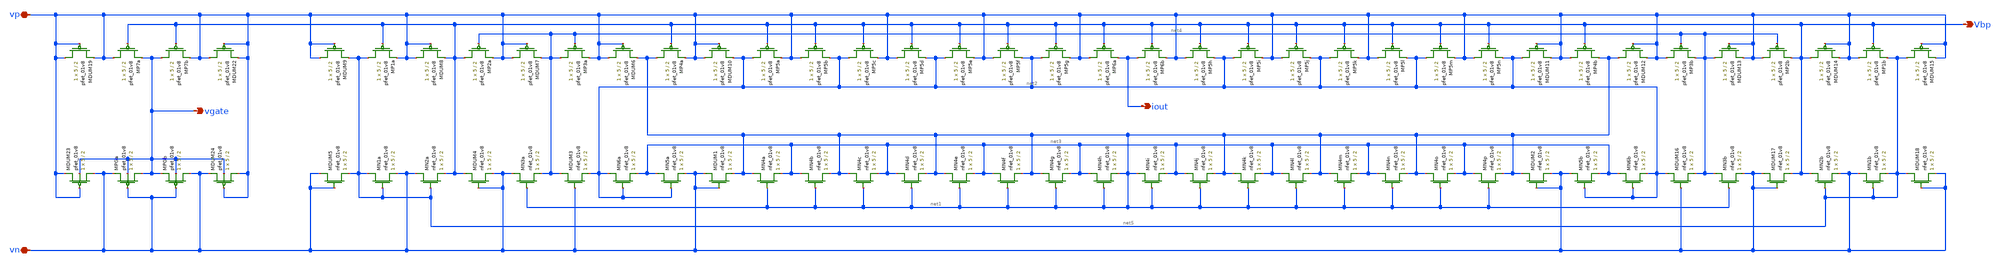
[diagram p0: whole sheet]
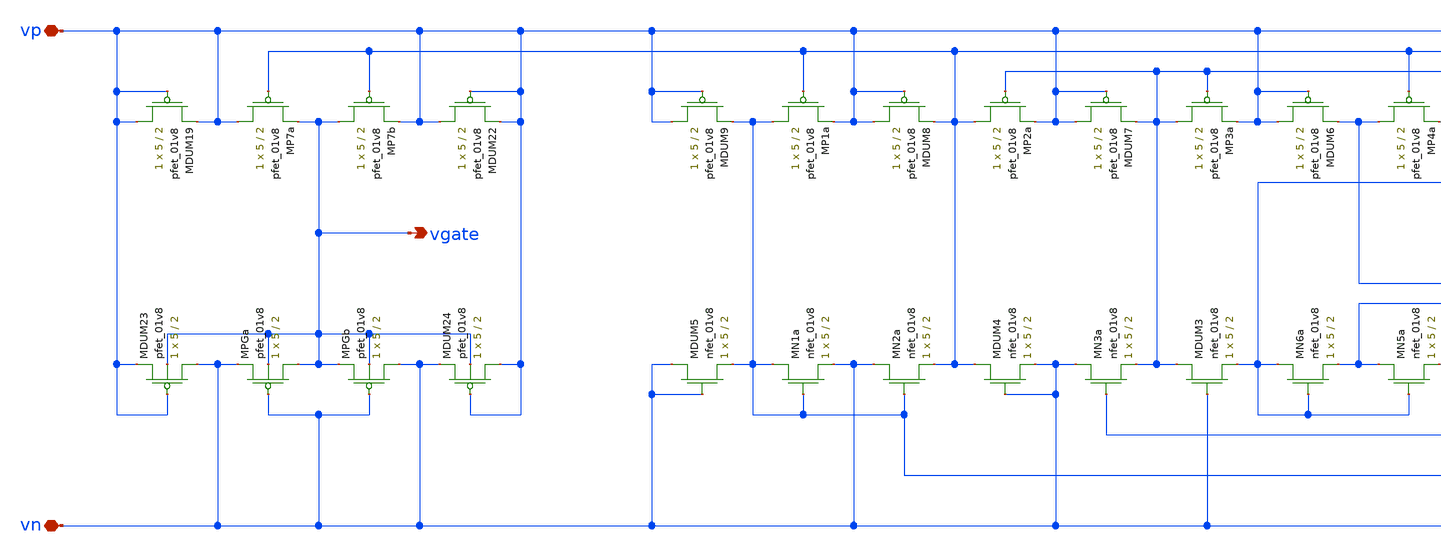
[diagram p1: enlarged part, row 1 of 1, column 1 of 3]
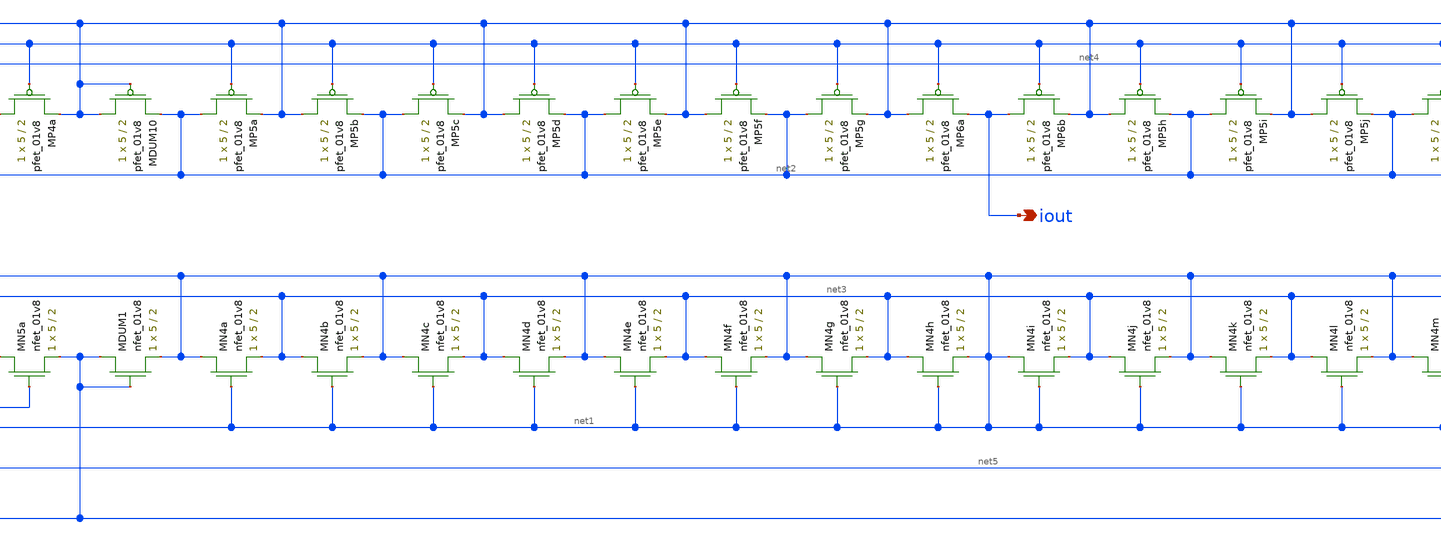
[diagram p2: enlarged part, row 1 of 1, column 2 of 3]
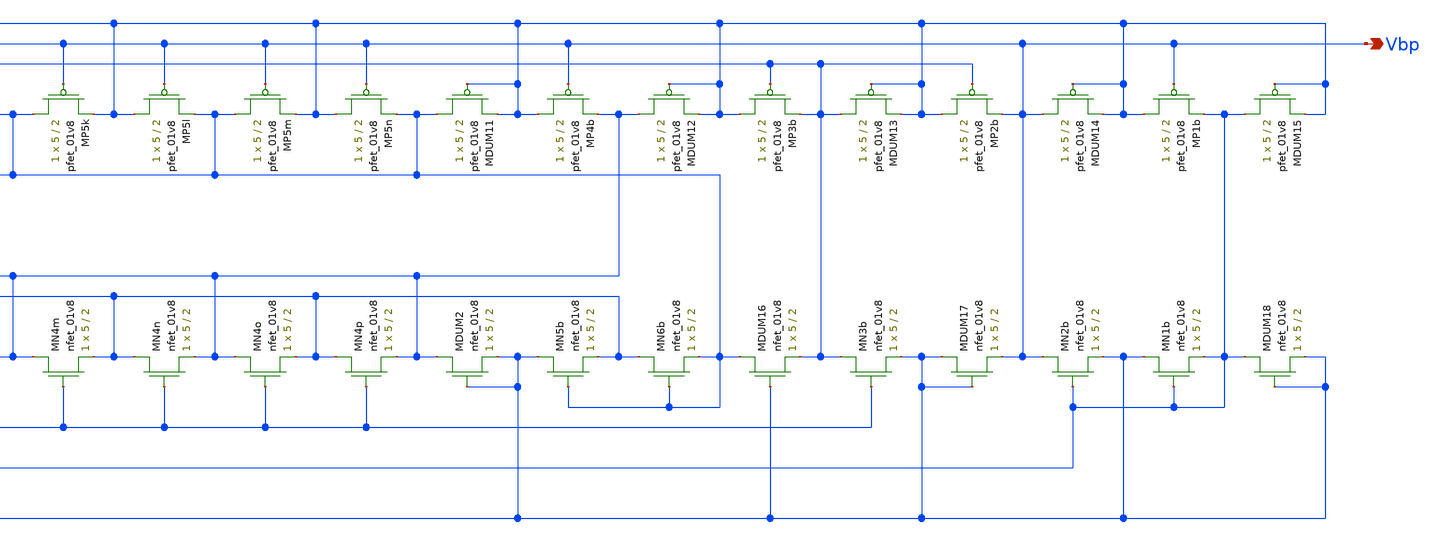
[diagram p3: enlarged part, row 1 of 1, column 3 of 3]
** sch_path: schematic/bias_current_LDS.sch
**.subckt bias_current_LDS iout Vbp vgate vp vn
*.opin iout
*.opin Vbp
*.opin vgate
*.iopin vp
*.iopin vn
XMP1a net5 Vbp vp VDD sky130_fd_pr__pfet_01v8 L=2 W=5 nf=1 ad='int((nf+1)/2) * W/nf * 0.29' as='int((nf+2)/2) * W/nf * 0.29'
+ pd='2*int((nf+1)/2) * (W/nf + 0.29)' ps='2*int((nf+2)/2) * (W/nf + 0.29)' nrd='0.29 / W' nrs='0.29 / W'
+ sa=0 sb=0 sd=0 mult=1 m=1
XMP1b vp Vbp net5 VDD sky130_fd_pr__pfet_01v8 L=2 W=5 nf=1 ad='int((nf+1)/2) * W/nf * 0.29' as='int((nf+2)/2) * W/nf * 0.29'
+ pd='2*int((nf+1)/2) * (W/nf + 0.29)' ps='2*int((nf+2)/2) * (W/nf + 0.29)' nrd='0.29 / W' nrs='0.29 / W'
+ sa=0 sb=0 sd=0 mult=1 m=1
XMP2a Vbp net4 vp VDD sky130_fd_pr__pfet_01v8 L=2 W=5 nf=1 ad='int((nf+1)/2) * W/nf * 0.29' as='int((nf+2)/2) * W/nf * 0.29'
+ pd='2*int((nf+1)/2) * (W/nf + 0.29)' ps='2*int((nf+2)/2) * (W/nf + 0.29)' nrd='0.29 / W' nrs='0.29 / W'
+ sa=0 sb=0 sd=0 mult=1 m=1
XMP2b vp net4 Vbp VDD sky130_fd_pr__pfet_01v8 L=2 W=5 nf=1 ad='int((nf+1)/2) * W/nf * 0.29' as='int((nf+2)/2) * W/nf * 0.29'
+ pd='2*int((nf+1)/2) * (W/nf + 0.29)' ps='2*int((nf+2)/2) * (W/nf + 0.29)' nrd='0.29 / W' nrs='0.29 / W'
+ sa=0 sb=0 sd=0 mult=1 m=1
XMP3a net4 net4 vp VDD sky130_fd_pr__pfet_01v8 L=2 W=5 nf=1 ad='int((nf+1)/2) * W/nf * 0.29' as='int((nf+2)/2) * W/nf * 0.29'
+ pd='2*int((nf+1)/2) * (W/nf + 0.29)' ps='2*int((nf+2)/2) * (W/nf + 0.29)' nrd='0.29 / W' nrs='0.29 / W'
+ sa=0 sb=0 sd=0 mult=1 m=1
XMP3b vp net4 net4 VDD sky130_fd_pr__pfet_01v8 L=2 W=5 nf=1 ad='int((nf+1)/2) * W/nf * 0.29' as='int((nf+2)/2) * W/nf * 0.29'
+ pd='2*int((nf+1)/2) * (W/nf + 0.29)' ps='2*int((nf+2)/2) * (W/nf + 0.29)' nrd='0.29 / W' nrs='0.29 / W'
+ sa=0 sb=0 sd=0 mult=1 m=1
XMP4a net1 Vbp vp VDD sky130_fd_pr__pfet_01v8 L=2 W=5 nf=1 ad='int((nf+1)/2) * W/nf * 0.29' as='int((nf+2)/2) * W/nf * 0.29'
+ pd='2*int((nf+1)/2) * (W/nf + 0.29)' ps='2*int((nf+2)/2) * (W/nf + 0.29)' nrd='0.29 / W' nrs='0.29 / W'
+ sa=0 sb=0 sd=0 mult=1 m=1
XMP4b vp Vbp net1 VDD sky130_fd_pr__pfet_01v8 L=2 W=5 nf=1 ad='int((nf+1)/2) * W/nf * 0.29' as='int((nf+2)/2) * W/nf * 0.29'
+ pd='2*int((nf+1)/2) * (W/nf + 0.29)' ps='2*int((nf+2)/2) * (W/nf + 0.29)' nrd='0.29 / W' nrs='0.29 / W'
+ sa=0 sb=0 sd=0 mult=1 m=1
XMN1a net5 net5 vn GND sky130_fd_pr__nfet_01v8 L=2 W=5 nf=1 ad='int((nf+1)/2) * W/nf * 0.29' as='int((nf+2)/2) * W/nf * 0.29'
+ pd='2*int((nf+1)/2) * (W/nf + 0.29)' ps='2*int((nf+2)/2) * (W/nf + 0.29)' nrd='0.29 / W' nrs='0.29 / W'
+ sa=0 sb=0 sd=0 mult=1 m=1
XMN1b vn net5 net5 GND sky130_fd_pr__nfet_01v8 L=2 W=5 nf=1 ad='int((nf+1)/2) * W/nf * 0.29' as='int((nf+2)/2) * W/nf * 0.29'
+ pd='2*int((nf+1)/2) * (W/nf + 0.29)' ps='2*int((nf+2)/2) * (W/nf + 0.29)' nrd='0.29 / W' nrs='0.29 / W'
+ sa=0 sb=0 sd=0 mult=1 m=1
XMN2a vn net5 Vbp GND sky130_fd_pr__nfet_01v8 L=2 W=5 nf=1 ad='int((nf+1)/2) * W/nf * 0.29' as='int((nf+2)/2) * W/nf * 0.29'
+ pd='2*int((nf+1)/2) * (W/nf + 0.29)' ps='2*int((nf+2)/2) * (W/nf + 0.29)' nrd='0.29 / W' nrs='0.29 / W'
+ sa=0 sb=0 sd=0 mult=1 m=1
XMN2b Vbp net5 vn GND sky130_fd_pr__nfet_01v8 L=2 W=5 nf=1 ad='int((nf+1)/2) * W/nf * 0.29' as='int((nf+2)/2) * W/nf * 0.29'
+ pd='2*int((nf+1)/2) * (W/nf + 0.29)' ps='2*int((nf+2)/2) * (W/nf + 0.29)' nrd='0.29 / W' nrs='0.29 / W'
+ sa=0 sb=0 sd=0 mult=1 m=1
XMN3a vn net1 net4 GND sky130_fd_pr__nfet_01v8 L=2 W=5 nf=1 ad='int((nf+1)/2) * W/nf * 0.29' as='int((nf+2)/2) * W/nf * 0.29'
+ pd='2*int((nf+1)/2) * (W/nf + 0.29)' ps='2*int((nf+2)/2) * (W/nf + 0.29)' nrd='0.29 / W' nrs='0.29 / W'
+ sa=0 sb=0 sd=0 mult=1 m=1
XMN3b net4 net1 vn GND sky130_fd_pr__nfet_01v8 L=2 W=5 nf=1 ad='int((nf+1)/2) * W/nf * 0.29' as='int((nf+2)/2) * W/nf * 0.29'
+ pd='2*int((nf+1)/2) * (W/nf + 0.29)' ps='2*int((nf+2)/2) * (W/nf + 0.29)' nrd='0.29 / W' nrs='0.29 / W'
+ sa=0 sb=0 sd=0 mult=1 m=1
XMN5a net3 net2 vn GND sky130_fd_pr__nfet_01v8 L=2 W=5 nf=1 ad='int((nf+1)/2) * W/nf * 0.29' as='int((nf+2)/2) * W/nf * 0.29'
+ pd='2*int((nf+1)/2) * (W/nf + 0.29)' ps='2*int((nf+2)/2) * (W/nf + 0.29)' nrd='0.29 / W' nrs='0.29 / W'
+ sa=0 sb=0 sd=0 mult=1 m=1
XMN5b vn net2 net3 GND sky130_fd_pr__nfet_01v8 L=2 W=5 nf=1 ad='int((nf+1)/2) * W/nf * 0.29' as='int((nf+2)/2) * W/nf * 0.29'
+ pd='2*int((nf+1)/2) * (W/nf + 0.29)' ps='2*int((nf+2)/2) * (W/nf + 0.29)' nrd='0.29 / W' nrs='0.29 / W'
+ sa=0 sb=0 sd=0 mult=1 m=1
XMN6a net2 net2 net3 GND sky130_fd_pr__nfet_01v8 L=2 W=5 nf=1 ad='int((nf+1)/2) * W/nf * 0.29' as='int((nf+2)/2) * W/nf * 0.29'
+ pd='2*int((nf+1)/2) * (W/nf + 0.29)' ps='2*int((nf+2)/2) * (W/nf + 0.29)' nrd='0.29 / W' nrs='0.29 / W'
+ sa=0 sb=0 sd=0 mult=1 m=1
XMN6b net3 net2 net2 GND sky130_fd_pr__nfet_01v8 L=2 W=5 nf=1 ad='int((nf+1)/2) * W/nf * 0.29' as='int((nf+2)/2) * W/nf * 0.29'
+ pd='2*int((nf+1)/2) * (W/nf + 0.29)' ps='2*int((nf+2)/2) * (W/nf + 0.29)' nrd='0.29 / W' nrs='0.29 / W'
+ sa=0 sb=0 sd=0 mult=1 m=1
XMP5g net2 Vbp vp VDD sky130_fd_pr__pfet_01v8 L=2 W=5 nf=1 ad='int((nf+1)/2) * W/nf * 0.29' as='int((nf+2)/2) * W/nf * 0.29'
+ pd='2*int((nf+1)/2) * (W/nf + 0.29)' ps='2*int((nf+2)/2) * (W/nf + 0.29)' nrd='0.29 / W' nrs='0.29 / W'
+ sa=0 sb=0 sd=0 mult=1 m=1
XMP5h vp Vbp net2 VDD sky130_fd_pr__pfet_01v8 L=2 W=5 nf=1 ad='int((nf+1)/2) * W/nf * 0.29' as='int((nf+2)/2) * W/nf * 0.29'
+ pd='2*int((nf+1)/2) * (W/nf + 0.29)' ps='2*int((nf+2)/2) * (W/nf + 0.29)' nrd='0.29 / W' nrs='0.29 / W'
+ sa=0 sb=0 sd=0 mult=1 m=1
XMP5a net2 Vbp vp VDD sky130_fd_pr__pfet_01v8 L=2 W=5 nf=1 ad='int((nf+1)/2) * W/nf * 0.29' as='int((nf+2)/2) * W/nf * 0.29'
+ pd='2*int((nf+1)/2) * (W/nf + 0.29)' ps='2*int((nf+2)/2) * (W/nf + 0.29)' nrd='0.29 / W' nrs='0.29 / W'
+ sa=0 sb=0 sd=0 mult=1 m=1
XMP5b vp Vbp net2 VDD sky130_fd_pr__pfet_01v8 L=2 W=5 nf=1 ad='int((nf+1)/2) * W/nf * 0.29' as='int((nf+2)/2) * W/nf * 0.29'
+ pd='2*int((nf+1)/2) * (W/nf + 0.29)' ps='2*int((nf+2)/2) * (W/nf + 0.29)' nrd='0.29 / W' nrs='0.29 / W'
+ sa=0 sb=0 sd=0 mult=1 m=1
XMP5c net2 Vbp vp VDD sky130_fd_pr__pfet_01v8 L=2 W=5 nf=1 ad='int((nf+1)/2) * W/nf * 0.29' as='int((nf+2)/2) * W/nf * 0.29'
+ pd='2*int((nf+1)/2) * (W/nf + 0.29)' ps='2*int((nf+2)/2) * (W/nf + 0.29)' nrd='0.29 / W' nrs='0.29 / W'
+ sa=0 sb=0 sd=0 mult=1 m=1
XMP5d vp Vbp net2 VDD sky130_fd_pr__pfet_01v8 L=2 W=5 nf=1 ad='int((nf+1)/2) * W/nf * 0.29' as='int((nf+2)/2) * W/nf * 0.29'
+ pd='2*int((nf+1)/2) * (W/nf + 0.29)' ps='2*int((nf+2)/2) * (W/nf + 0.29)' nrd='0.29 / W' nrs='0.29 / W'
+ sa=0 sb=0 sd=0 mult=1 m=1
XMP5e net2 Vbp vp VDD sky130_fd_pr__pfet_01v8 L=2 W=5 nf=1 ad='int((nf+1)/2) * W/nf * 0.29' as='int((nf+2)/2) * W/nf * 0.29'
+ pd='2*int((nf+1)/2) * (W/nf + 0.29)' ps='2*int((nf+2)/2) * (W/nf + 0.29)' nrd='0.29 / W' nrs='0.29 / W'
+ sa=0 sb=0 sd=0 mult=1 m=1
XMP5f vp Vbp net2 VDD sky130_fd_pr__pfet_01v8 L=2 W=5 nf=1 ad='int((nf+1)/2) * W/nf * 0.29' as='int((nf+2)/2) * W/nf * 0.29'
+ pd='2*int((nf+1)/2) * (W/nf + 0.29)' ps='2*int((nf+2)/2) * (W/nf + 0.29)' nrd='0.29 / W' nrs='0.29 / W'
+ sa=0 sb=0 sd=0 mult=1 m=1
XMP5i net2 Vbp vp VDD sky130_fd_pr__pfet_01v8 L=2 W=5 nf=1 ad='int((nf+1)/2) * W/nf * 0.29' as='int((nf+2)/2) * W/nf * 0.29'
+ pd='2*int((nf+1)/2) * (W/nf + 0.29)' ps='2*int((nf+2)/2) * (W/nf + 0.29)' nrd='0.29 / W' nrs='0.29 / W'
+ sa=0 sb=0 sd=0 mult=1 m=1
XMP5j vp Vbp net2 VDD sky130_fd_pr__pfet_01v8 L=2 W=5 nf=1 ad='int((nf+1)/2) * W/nf * 0.29' as='int((nf+2)/2) * W/nf * 0.29'
+ pd='2*int((nf+1)/2) * (W/nf + 0.29)' ps='2*int((nf+2)/2) * (W/nf + 0.29)' nrd='0.29 / W' nrs='0.29 / W'
+ sa=0 sb=0 sd=0 mult=1 m=1
XMP5k net2 Vbp vp VDD sky130_fd_pr__pfet_01v8 L=2 W=5 nf=1 ad='int((nf+1)/2) * W/nf * 0.29' as='int((nf+2)/2) * W/nf * 0.29'
+ pd='2*int((nf+1)/2) * (W/nf + 0.29)' ps='2*int((nf+2)/2) * (W/nf + 0.29)' nrd='0.29 / W' nrs='0.29 / W'
+ sa=0 sb=0 sd=0 mult=1 m=1
XMP5l vp Vbp net2 VDD sky130_fd_pr__pfet_01v8 L=2 W=5 nf=1 ad='int((nf+1)/2) * W/nf * 0.29' as='int((nf+2)/2) * W/nf * 0.29'
+ pd='2*int((nf+1)/2) * (W/nf + 0.29)' ps='2*int((nf+2)/2) * (W/nf + 0.29)' nrd='0.29 / W' nrs='0.29 / W'
+ sa=0 sb=0 sd=0 mult=1 m=1
XMP5m net2 Vbp vp VDD sky130_fd_pr__pfet_01v8 L=2 W=5 nf=1 ad='int((nf+1)/2) * W/nf * 0.29' as='int((nf+2)/2) * W/nf * 0.29'
+ pd='2*int((nf+1)/2) * (W/nf + 0.29)' ps='2*int((nf+2)/2) * (W/nf + 0.29)' nrd='0.29 / W' nrs='0.29 / W'
+ sa=0 sb=0 sd=0 mult=1 m=1
XMP5n vp Vbp net2 VDD sky130_fd_pr__pfet_01v8 L=2 W=5 nf=1 ad='int((nf+1)/2) * W/nf * 0.29' as='int((nf+2)/2) * W/nf * 0.29'
+ pd='2*int((nf+1)/2) * (W/nf + 0.29)' ps='2*int((nf+2)/2) * (W/nf + 0.29)' nrd='0.29 / W' nrs='0.29 / W'
+ sa=0 sb=0 sd=0 mult=1 m=1
XMP7a vp Vbp vgate VDD sky130_fd_pr__pfet_01v8 L=2 W=5 nf=1 ad='int((nf+1)/2) * W/nf * 0.29' as='int((nf+2)/2) * W/nf * 0.29'
+ pd='2*int((nf+1)/2) * (W/nf + 0.29)' ps='2*int((nf+2)/2) * (W/nf + 0.29)' nrd='0.29 / W' nrs='0.29 / W'
+ sa=0 sb=0 sd=0 mult=1 m=1
XMDUM1 vn vn net1 GND sky130_fd_pr__nfet_01v8 L=2 W=5 nf=1 ad='int((nf+1)/2) * W/nf * 0.29' as='int((nf+2)/2) * W/nf * 0.29'
+ pd='2*int((nf+1)/2) * (W/nf + 0.29)' ps='2*int((nf+2)/2) * (W/nf + 0.29)' nrd='0.29 / W' nrs='0.29 / W'
+ sa=0 sb=0 sd=0 mult=1 m=1
XMN4a net1 net1 net3 GND sky130_fd_pr__nfet_01v8 L=2 W=5 nf=1 ad='int((nf+1)/2) * W/nf * 0.29' as='int((nf+2)/2) * W/nf * 0.29'
+ pd='2*int((nf+1)/2) * (W/nf + 0.29)' ps='2*int((nf+2)/2) * (W/nf + 0.29)' nrd='0.29 / W' nrs='0.29 / W'
+ sa=0 sb=0 sd=0 mult=1 m=1
XMN4b net3 net1 net1 GND sky130_fd_pr__nfet_01v8 L=2 W=5 nf=1 ad='int((nf+1)/2) * W/nf * 0.29' as='int((nf+2)/2) * W/nf * 0.29'
+ pd='2*int((nf+1)/2) * (W/nf + 0.29)' ps='2*int((nf+2)/2) * (W/nf + 0.29)' nrd='0.29 / W' nrs='0.29 / W'
+ sa=0 sb=0 sd=0 mult=1 m=1
XMN4c net1 net1 net3 GND sky130_fd_pr__nfet_01v8 L=2 W=5 nf=1 ad='int((nf+1)/2) * W/nf * 0.29' as='int((nf+2)/2) * W/nf * 0.29'
+ pd='2*int((nf+1)/2) * (W/nf + 0.29)' ps='2*int((nf+2)/2) * (W/nf + 0.29)' nrd='0.29 / W' nrs='0.29 / W'
+ sa=0 sb=0 sd=0 mult=1 m=1
XMN4d net3 net1 net1 GND sky130_fd_pr__nfet_01v8 L=2 W=5 nf=1 ad='int((nf+1)/2) * W/nf * 0.29' as='int((nf+2)/2) * W/nf * 0.29'
+ pd='2*int((nf+1)/2) * (W/nf + 0.29)' ps='2*int((nf+2)/2) * (W/nf + 0.29)' nrd='0.29 / W' nrs='0.29 / W'
+ sa=0 sb=0 sd=0 mult=1 m=1
XMN4e net1 net1 net3 GND sky130_fd_pr__nfet_01v8 L=2 W=5 nf=1 ad='int((nf+1)/2) * W/nf * 0.29' as='int((nf+2)/2) * W/nf * 0.29'
+ pd='2*int((nf+1)/2) * (W/nf + 0.29)' ps='2*int((nf+2)/2) * (W/nf + 0.29)' nrd='0.29 / W' nrs='0.29 / W'
+ sa=0 sb=0 sd=0 mult=1 m=1
XMN4f net3 net1 net1 GND sky130_fd_pr__nfet_01v8 L=2 W=5 nf=1 ad='int((nf+1)/2) * W/nf * 0.29' as='int((nf+2)/2) * W/nf * 0.29'
+ pd='2*int((nf+1)/2) * (W/nf + 0.29)' ps='2*int((nf+2)/2) * (W/nf + 0.29)' nrd='0.29 / W' nrs='0.29 / W'
+ sa=0 sb=0 sd=0 mult=1 m=1
XMN4i net1 net1 net3 GND sky130_fd_pr__nfet_01v8 L=2 W=5 nf=1 ad='int((nf+1)/2) * W/nf * 0.29' as='int((nf+2)/2) * W/nf * 0.29'
+ pd='2*int((nf+1)/2) * (W/nf + 0.29)' ps='2*int((nf+2)/2) * (W/nf + 0.29)' nrd='0.29 / W' nrs='0.29 / W'
+ sa=0 sb=0 sd=0 mult=1 m=1
XMN4g net1 net1 net3 GND sky130_fd_pr__nfet_01v8 L=2 W=5 nf=1 ad='int((nf+1)/2) * W/nf * 0.29' as='int((nf+2)/2) * W/nf * 0.29'
+ pd='2*int((nf+1)/2) * (W/nf + 0.29)' ps='2*int((nf+2)/2) * (W/nf + 0.29)' nrd='0.29 / W' nrs='0.29 / W'
+ sa=0 sb=0 sd=0 mult=1 m=1
XMN4h net3 net1 net1 GND sky130_fd_pr__nfet_01v8 L=2 W=5 nf=1 ad='int((nf+1)/2) * W/nf * 0.29' as='int((nf+2)/2) * W/nf * 0.29'
+ pd='2*int((nf+1)/2) * (W/nf + 0.29)' ps='2*int((nf+2)/2) * (W/nf + 0.29)' nrd='0.29 / W' nrs='0.29 / W'
+ sa=0 sb=0 sd=0 mult=1 m=1
XMN4j net3 net1 net1 GND sky130_fd_pr__nfet_01v8 L=2 W=5 nf=1 ad='int((nf+1)/2) * W/nf * 0.29' as='int((nf+2)/2) * W/nf * 0.29'
+ pd='2*int((nf+1)/2) * (W/nf + 0.29)' ps='2*int((nf+2)/2) * (W/nf + 0.29)' nrd='0.29 / W' nrs='0.29 / W'
+ sa=0 sb=0 sd=0 mult=1 m=1
XMN4k net1 net1 net3 GND sky130_fd_pr__nfet_01v8 L=2 W=5 nf=1 ad='int((nf+1)/2) * W/nf * 0.29' as='int((nf+2)/2) * W/nf * 0.29'
+ pd='2*int((nf+1)/2) * (W/nf + 0.29)' ps='2*int((nf+2)/2) * (W/nf + 0.29)' nrd='0.29 / W' nrs='0.29 / W'
+ sa=0 sb=0 sd=0 mult=1 m=1
XMN4l net3 net1 net1 GND sky130_fd_pr__nfet_01v8 L=2 W=5 nf=1 ad='int((nf+1)/2) * W/nf * 0.29' as='int((nf+2)/2) * W/nf * 0.29'
+ pd='2*int((nf+1)/2) * (W/nf + 0.29)' ps='2*int((nf+2)/2) * (W/nf + 0.29)' nrd='0.29 / W' nrs='0.29 / W'
+ sa=0 sb=0 sd=0 mult=1 m=1
XMN4m net1 net1 net3 GND sky130_fd_pr__nfet_01v8 L=2 W=5 nf=1 ad='int((nf+1)/2) * W/nf * 0.29' as='int((nf+2)/2) * W/nf * 0.29'
+ pd='2*int((nf+1)/2) * (W/nf + 0.29)' ps='2*int((nf+2)/2) * (W/nf + 0.29)' nrd='0.29 / W' nrs='0.29 / W'
+ sa=0 sb=0 sd=0 mult=1 m=1
XMN4p net3 net1 net1 GND sky130_fd_pr__nfet_01v8 L=2 W=5 nf=1 ad='int((nf+1)/2) * W/nf * 0.29' as='int((nf+2)/2) * W/nf * 0.29'
+ pd='2*int((nf+1)/2) * (W/nf + 0.29)' ps='2*int((nf+2)/2) * (W/nf + 0.29)' nrd='0.29 / W' nrs='0.29 / W'
+ sa=0 sb=0 sd=0 mult=1 m=1
XMN4n net3 net1 net1 GND sky130_fd_pr__nfet_01v8 L=2 W=5 nf=1 ad='int((nf+1)/2) * W/nf * 0.29' as='int((nf+2)/2) * W/nf * 0.29'
+ pd='2*int((nf+1)/2) * (W/nf + 0.29)' ps='2*int((nf+2)/2) * (W/nf + 0.29)' nrd='0.29 / W' nrs='0.29 / W'
+ sa=0 sb=0 sd=0 mult=1 m=1
XMN4o net1 net1 net3 GND sky130_fd_pr__nfet_01v8 L=2 W=5 nf=1 ad='int((nf+1)/2) * W/nf * 0.29' as='int((nf+2)/2) * W/nf * 0.29'
+ pd='2*int((nf+1)/2) * (W/nf + 0.29)' ps='2*int((nf+2)/2) * (W/nf + 0.29)' nrd='0.29 / W' nrs='0.29 / W'
+ sa=0 sb=0 sd=0 mult=1 m=1
XMDUM2 net1 vn vn GND sky130_fd_pr__nfet_01v8 L=2 W=5 nf=1 ad='int((nf+1)/2) * W/nf * 0.29' as='int((nf+2)/2) * W/nf * 0.29'
+ pd='2*int((nf+1)/2) * (W/nf + 0.29)' ps='2*int((nf+2)/2) * (W/nf + 0.29)' nrd='0.29 / W' nrs='0.29 / W'
+ sa=0 sb=0 sd=0 mult=1 m=1
XMDUM3 net4 vn net2 GND sky130_fd_pr__nfet_01v8 L=2 W=5 nf=1 ad='int((nf+1)/2) * W/nf * 0.29' as='int((nf+2)/2) * W/nf * 0.29'
+ pd='2*int((nf+1)/2) * (W/nf + 0.29)' ps='2*int((nf+2)/2) * (W/nf + 0.29)' nrd='0.29 / W' nrs='0.29 / W'
+ sa=0 sb=0 sd=0 mult=1 m=1
XMDUM4 Vbp vn vn GND sky130_fd_pr__nfet_01v8 L=2 W=5 nf=1 ad='int((nf+1)/2) * W/nf * 0.29' as='int((nf+2)/2) * W/nf * 0.29'
+ pd='2*int((nf+1)/2) * (W/nf + 0.29)' ps='2*int((nf+2)/2) * (W/nf + 0.29)' nrd='0.29 / W' nrs='0.29 / W'
+ sa=0 sb=0 sd=0 mult=1 m=1
XMDUM5 vn vn net5 GND sky130_fd_pr__nfet_01v8 L=2 W=5 nf=1 ad='int((nf+1)/2) * W/nf * 0.29' as='int((nf+2)/2) * W/nf * 0.29'
+ pd='2*int((nf+1)/2) * (W/nf + 0.29)' ps='2*int((nf+2)/2) * (W/nf + 0.29)' nrd='0.29 / W' nrs='0.29 / W'
+ sa=0 sb=0 sd=0 mult=1 m=1
XMDUM6 vp vp net1 VDD sky130_fd_pr__pfet_01v8 L=2 W=5 nf=1 ad='int((nf+1)/2) * W/nf * 0.29' as='int((nf+2)/2) * W/nf * 0.29'
+ pd='2*int((nf+1)/2) * (W/nf + 0.29)' ps='2*int((nf+2)/2) * (W/nf + 0.29)' nrd='0.29 / W' nrs='0.29 / W'
+ sa=0 sb=0 sd=0 mult=1 m=1
XMDUM7 vp vp net4 VDD sky130_fd_pr__pfet_01v8 L=2 W=5 nf=1 ad='int((nf+1)/2) * W/nf * 0.29' as='int((nf+2)/2) * W/nf * 0.29'
+ pd='2*int((nf+1)/2) * (W/nf + 0.29)' ps='2*int((nf+2)/2) * (W/nf + 0.29)' nrd='0.29 / W' nrs='0.29 / W'
+ sa=0 sb=0 sd=0 mult=1 m=1
XMDUM8 vp vp Vbp VDD sky130_fd_pr__pfet_01v8 L=2 W=5 nf=1 ad='int((nf+1)/2) * W/nf * 0.29' as='int((nf+2)/2) * W/nf * 0.29'
+ pd='2*int((nf+1)/2) * (W/nf + 0.29)' ps='2*int((nf+2)/2) * (W/nf + 0.29)' nrd='0.29 / W' nrs='0.29 / W'
+ sa=0 sb=0 sd=0 mult=1 m=1
XMDUM9 vp vp net5 VDD sky130_fd_pr__pfet_01v8 L=2 W=5 nf=1 ad='int((nf+1)/2) * W/nf * 0.29' as='int((nf+2)/2) * W/nf * 0.29'
+ pd='2*int((nf+1)/2) * (W/nf + 0.29)' ps='2*int((nf+2)/2) * (W/nf + 0.29)' nrd='0.29 / W' nrs='0.29 / W'
+ sa=0 sb=0 sd=0 mult=1 m=1
XMDUM10 vp vp net2 VDD sky130_fd_pr__pfet_01v8 L=2 W=5 nf=1 ad='int((nf+1)/2) * W/nf * 0.29' as='int((nf+2)/2) * W/nf * 0.29'
+ pd='2*int((nf+1)/2) * (W/nf + 0.29)' ps='2*int((nf+2)/2) * (W/nf + 0.29)' nrd='0.29 / W' nrs='0.29 / W'
+ sa=0 sb=0 sd=0 mult=1 m=1
XMDUM11 net2 vp vp VDD sky130_fd_pr__pfet_01v8 L=2 W=5 nf=1 ad='int((nf+1)/2) * W/nf * 0.29' as='int((nf+2)/2) * W/nf * 0.29'
+ pd='2*int((nf+1)/2) * (W/nf + 0.29)' ps='2*int((nf+2)/2) * (W/nf + 0.29)' nrd='0.29 / W' nrs='0.29 / W'
+ sa=0 sb=0 sd=0 mult=1 m=1
XMP6a vp Vbp iout VDD sky130_fd_pr__pfet_01v8 L=2 W=5 nf=1 ad='int((nf+1)/2) * W/nf * 0.29' as='int((nf+2)/2) * W/nf * 0.29'
+ pd='2*int((nf+1)/2) * (W/nf + 0.29)' ps='2*int((nf+2)/2) * (W/nf + 0.29)' nrd='0.29 / W' nrs='0.29 / W'
+ sa=0 sb=0 sd=0 mult=1 m=1
XMP6b iout Vbp vp VDD sky130_fd_pr__pfet_01v8 L=2 W=5 nf=1 ad='int((nf+1)/2) * W/nf * 0.29' as='int((nf+2)/2) * W/nf * 0.29'
+ pd='2*int((nf+1)/2) * (W/nf + 0.29)' ps='2*int((nf+2)/2) * (W/nf + 0.29)' nrd='0.29 / W' nrs='0.29 / W'
+ sa=0 sb=0 sd=0 mult=1 m=1
XMDUM12 net1 vp vp VDD sky130_fd_pr__pfet_01v8 L=2 W=5 nf=1 ad='int((nf+1)/2) * W/nf * 0.29' as='int((nf+2)/2) * W/nf * 0.29'
+ pd='2*int((nf+1)/2) * (W/nf + 0.29)' ps='2*int((nf+2)/2) * (W/nf + 0.29)' nrd='0.29 / W' nrs='0.29 / W'
+ sa=0 sb=0 sd=0 mult=1 m=1
XMDUM13 net4 vp vp VDD sky130_fd_pr__pfet_01v8 L=2 W=5 nf=1 ad='int((nf+1)/2) * W/nf * 0.29' as='int((nf+2)/2) * W/nf * 0.29'
+ pd='2*int((nf+1)/2) * (W/nf + 0.29)' ps='2*int((nf+2)/2) * (W/nf + 0.29)' nrd='0.29 / W' nrs='0.29 / W'
+ sa=0 sb=0 sd=0 mult=1 m=1
XMDUM14 Vbp vp vp VDD sky130_fd_pr__pfet_01v8 L=2 W=5 nf=1 ad='int((nf+1)/2) * W/nf * 0.29' as='int((nf+2)/2) * W/nf * 0.29'
+ pd='2*int((nf+1)/2) * (W/nf + 0.29)' ps='2*int((nf+2)/2) * (W/nf + 0.29)' nrd='0.29 / W' nrs='0.29 / W'
+ sa=0 sb=0 sd=0 mult=1 m=1
XMDUM15 net5 vp vp VDD sky130_fd_pr__pfet_01v8 L=2 W=5 nf=1 ad='int((nf+1)/2) * W/nf * 0.29' as='int((nf+2)/2) * W/nf * 0.29'
+ pd='2*int((nf+1)/2) * (W/nf + 0.29)' ps='2*int((nf+2)/2) * (W/nf + 0.29)' nrd='0.29 / W' nrs='0.29 / W'
+ sa=0 sb=0 sd=0 mult=1 m=1
XMDUM16 net2 vn net4 GND sky130_fd_pr__nfet_01v8 L=2 W=5 nf=1 ad='int((nf+1)/2) * W/nf * 0.29' as='int((nf+2)/2) * W/nf * 0.29'
+ pd='2*int((nf+1)/2) * (W/nf + 0.29)' ps='2*int((nf+2)/2) * (W/nf + 0.29)' nrd='0.29 / W' nrs='0.29 / W'
+ sa=0 sb=0 sd=0 mult=1 m=1
XMDUM17 vn vn Vbp GND sky130_fd_pr__nfet_01v8 L=2 W=5 nf=1 ad='int((nf+1)/2) * W/nf * 0.29' as='int((nf+2)/2) * W/nf * 0.29'
+ pd='2*int((nf+1)/2) * (W/nf + 0.29)' ps='2*int((nf+2)/2) * (W/nf + 0.29)' nrd='0.29 / W' nrs='0.29 / W'
+ sa=0 sb=0 sd=0 mult=1 m=1
XMDUM18 net5 vn vn GND sky130_fd_pr__nfet_01v8 L=2 W=5 nf=1 ad='int((nf+1)/2) * W/nf * 0.29' as='int((nf+2)/2) * W/nf * 0.29'
+ pd='2*int((nf+1)/2) * (W/nf + 0.29)' ps='2*int((nf+2)/2) * (W/nf + 0.29)' nrd='0.29 / W' nrs='0.29 / W'
+ sa=0 sb=0 sd=0 mult=1 m=1
XMDUM19 vp vp vp VDD sky130_fd_pr__pfet_01v8 L=2 W=5 nf=1 ad='int((nf+1)/2) * W/nf * 0.29' as='int((nf+2)/2) * W/nf * 0.29'
+ pd='2*int((nf+1)/2) * (W/nf + 0.29)' ps='2*int((nf+2)/2) * (W/nf + 0.29)' nrd='0.29 / W' nrs='0.29 / W'
+ sa=0 sb=0 sd=0 mult=1 m=1
XMPGa vgate vn vn vgate sky130_fd_pr__pfet_01v8 L=2 W=5 nf=1 ad='int((nf+1)/2) * W/nf * 0.29' as='int((nf+2)/2) * W/nf * 0.29'
+ pd='2*int((nf+1)/2) * (W/nf + 0.29)' ps='2*int((nf+2)/2) * (W/nf + 0.29)' nrd='0.29 / W' nrs='0.29 / W'
+ sa=0 sb=0 sd=0 mult=1 m=1
XMP7b vgate Vbp vp VDD sky130_fd_pr__pfet_01v8 L=2 W=5 nf=1 ad='int((nf+1)/2) * W/nf * 0.29' as='int((nf+2)/2) * W/nf * 0.29'
+ pd='2*int((nf+1)/2) * (W/nf + 0.29)' ps='2*int((nf+2)/2) * (W/nf + 0.29)' nrd='0.29 / W' nrs='0.29 / W'
+ sa=0 sb=0 sd=0 mult=1 m=1
XMPGb vn vn vgate vgate sky130_fd_pr__pfet_01v8 L=2 W=5 nf=1 ad='int((nf+1)/2) * W/nf * 0.29' as='int((nf+2)/2) * W/nf * 0.29'
+ pd='2*int((nf+1)/2) * (W/nf + 0.29)' ps='2*int((nf+2)/2) * (W/nf + 0.29)' nrd='0.29 / W' nrs='0.29 / W'
+ sa=0 sb=0 sd=0 mult=1 m=1
XMDUM22 vp vp vp VDD sky130_fd_pr__pfet_01v8 L=2 W=5 nf=1 ad='int((nf+1)/2) * W/nf * 0.29' as='int((nf+2)/2) * W/nf * 0.29'
+ pd='2*int((nf+1)/2) * (W/nf + 0.29)' ps='2*int((nf+2)/2) * (W/nf + 0.29)' nrd='0.29 / W' nrs='0.29 / W'
+ sa=0 sb=0 sd=0 mult=1 m=1
XMDUM23 vn vp vp vgate sky130_fd_pr__pfet_01v8 L=2 W=5 nf=1 ad='int((nf+1)/2) * W/nf * 0.29' as='int((nf+2)/2) * W/nf * 0.29'
+ pd='2*int((nf+1)/2) * (W/nf + 0.29)' ps='2*int((nf+2)/2) * (W/nf + 0.29)' nrd='0.29 / W' nrs='0.29 / W'
+ sa=0 sb=0 sd=0 mult=1 m=1
XMDUM24 vp vp vn vgate sky130_fd_pr__pfet_01v8 L=2 W=5 nf=1 ad='int((nf+1)/2) * W/nf * 0.29' as='int((nf+2)/2) * W/nf * 0.29'
+ pd='2*int((nf+1)/2) * (W/nf + 0.29)' ps='2*int((nf+2)/2) * (W/nf + 0.29)' nrd='0.29 / W' nrs='0.29 / W'
+ sa=0 sb=0 sd=0 mult=1 m=1
**.ends
.end
